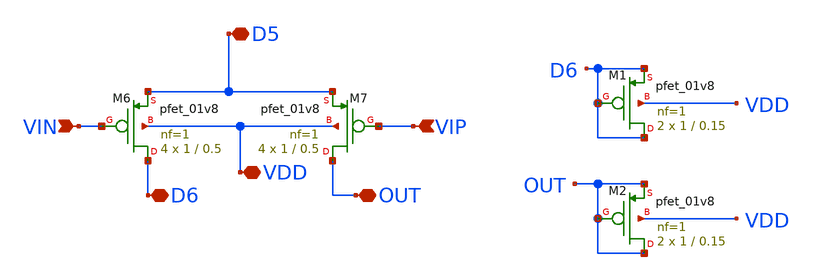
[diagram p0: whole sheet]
** sch_path: Op-Amp/mag/pmos_diff_amp.sch
**.subckt pmos_diff_amp VIN VIP D6 D5 VDD OUT
*.ipin VIN
*.ipin VIP
*.iopin D6
*.iopin D5
*.iopin VDD
*.iopin OUT
XM6 D6 VIN D5 VDD sky130_fd_pr__pfet_01v8 L=0.5 W=1 nf=1 ad='int((nf+1)/2) * W/nf * 0.29' as='int((nf+2)/2) * W/nf * 0.29'
+ pd='2*int((nf+1)/2) * (W/nf + 0.29)' ps='2*int((nf+2)/2) * (W/nf + 0.29)' nrd='0.29 / W' nrs='0.29 / W'
+ sa=0 sb=0 sd=0 mult=4 m=4
XM7 OUT VIP D5 VDD sky130_fd_pr__pfet_01v8 L=0.5 W=1 nf=1 ad='int((nf+1)/2) * W/nf * 0.29' as='int((nf+2)/2) * W/nf * 0.29'
+ pd='2*int((nf+1)/2) * (W/nf + 0.29)' ps='2*int((nf+2)/2) * (W/nf + 0.29)' nrd='0.29 / W' nrs='0.29 / W'
+ sa=0 sb=0 sd=0 mult=4 m=4
XM1 D6 D6 D6 VDD sky130_fd_pr__pfet_01v8 L=0.15 W=1 nf=1 ad='int((nf+1)/2) * W/nf * 0.29' as='int((nf+2)/2) * W/nf * 0.29'
+ pd='2*int((nf+1)/2) * (W/nf + 0.29)' ps='2*int((nf+2)/2) * (W/nf + 0.29)' nrd='0.29 / W' nrs='0.29 / W'
+ sa=0 sb=0 sd=0 mult=2 m=2
XM2 OUT OUT OUT VDD sky130_fd_pr__pfet_01v8 L=0.15 W=1 nf=1 ad='int((nf+1)/2) * W/nf * 0.29' as='int((nf+2)/2) * W/nf * 0.29'
+ pd='2*int((nf+1)/2) * (W/nf + 0.29)' ps='2*int((nf+2)/2) * (W/nf + 0.29)' nrd='0.29 / W' nrs='0.29 / W'
+ sa=0 sb=0 sd=0 mult=2 m=2
**.ends
.end
